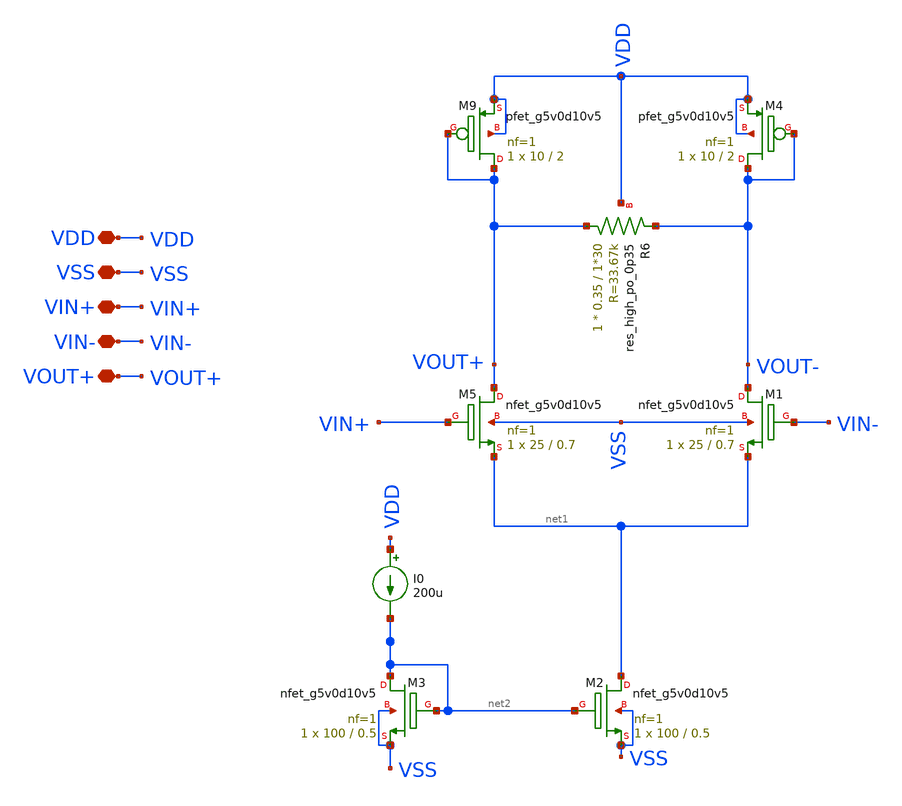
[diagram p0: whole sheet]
** sch_path: amplifiers/differencial_stage_amps/stange stages/with a resistor_stage/differential_stage.sch
**.subckt differential_stage VDD VSS VIN+ VIN- VOUT+
*.iopin VDD
*.iopin VSS
*.iopin VIN+
*.iopin VIN-
*.iopin VOUT+
XM5 VOUT+ VIN+ net1 VSS sky130_fd_pr__nfet_g5v0d10v5 L=0.7 W=25 nf=1 ad='int((1 + 1)/2) * 25 / 1 * 0.29'
+ as='int((1 + 2)/2) * 25 / 1 * 0.29' pd='2*int((1 + 1)/2) * (25 / 1 + 0.29)' ps='2*int((1 + 2)/2) * (25 / 1 + 0.29)'
+ nrd='0.29 / 25 ' nrs='0.29 / 25 ' sa=0 sb=0 sd=0 mult=1 m=1
XM1 VOUT- VIN- net1 VSS sky130_fd_pr__nfet_g5v0d10v5 L=0.7 W=25 nf=1 ad='int((1 + 1)/2) * 25 / 1 * 0.29'
+ as='int((1 + 2)/2) * 25 / 1 * 0.29' pd='2*int((1 + 1)/2) * (25 / 1 + 0.29)' ps='2*int((1 + 2)/2) * (25 / 1 + 0.29)'
+ nrd='0.29 / 25 ' nrs='0.29 / 25 ' sa=0 sb=0 sd=0 mult=1 m=1
XM2 net1 net2 VSS VSS sky130_fd_pr__nfet_g5v0d10v5 L=0.5 W=100 nf=1 ad='int((1 + 1)/2) * 100 / 1 * 0.29'
+ as='int((1 + 2)/2) * 100 / 1 * 0.29' pd='2*int((1 + 1)/2) * (100 / 1 + 0.29)' ps='2*int((1 + 2)/2) * (100 / 1 + 0.29)'
+ nrd='0.29 / 100 ' nrs='0.29 / 100 ' sa=0 sb=0 sd=0 mult=1 m=1
XM3 net2 net2 VSS VSS sky130_fd_pr__nfet_g5v0d10v5 L=0.5 W=100 nf=1 ad='int((1 + 1)/2) * 100 / 1 * 0.29'
+ as='int((1 + 2)/2) * 100 / 1 * 0.29' pd='2*int((1 + 1)/2) * (100 / 1 + 0.29)' ps='2*int((1 + 2)/2) * (100 / 1 + 0.29)'
+ nrd='0.29 / 100 ' nrs='0.29 / 100 ' sa=0 sb=0 sd=0 mult=1 m=1
I0 VDD net2 200u
XM9 VOUT+ VOUT+ VDD VDD sky130_fd_pr__pfet_g5v0d10v5 L=2 W=10 nf=1 ad='int((1 + 1)/2) * 10 / 1 * 0.29'
+ as='int((1 + 2)/2) * 10 / 1 * 0.29' pd='2*int((1 + 1)/2) * (10 / 1 + 0.29)' ps='2*int((1 + 2)/2) * (10 / 1 + 0.29)'
+ nrd='0.29 / 10 ' nrs='0.29 / 10 ' sa=0 sb=0 sd=0 mult=1 m=1
XM4 VOUT- VOUT- VDD VDD sky130_fd_pr__pfet_g5v0d10v5 L=2 W=10 nf=1 ad='int((1 + 1)/2) * 10 / 1 * 0.29'
+ as='int((1 + 2)/2) * 10 / 1 * 0.29' pd='2*int((1 + 1)/2) * (10 / 1 + 0.29)' ps='2*int((1 + 2)/2) * (10 / 1 + 0.29)'
+ nrd='0.29 / 10 ' nrs='0.29 / 10 ' sa=0 sb=0 sd=0 mult=1 m=1
XR6 VOUT+ VOUT- VDD sky130_fd_pr__res_high_po_0p35 L=1*30 mult=1 m=1
**.ends
.end
